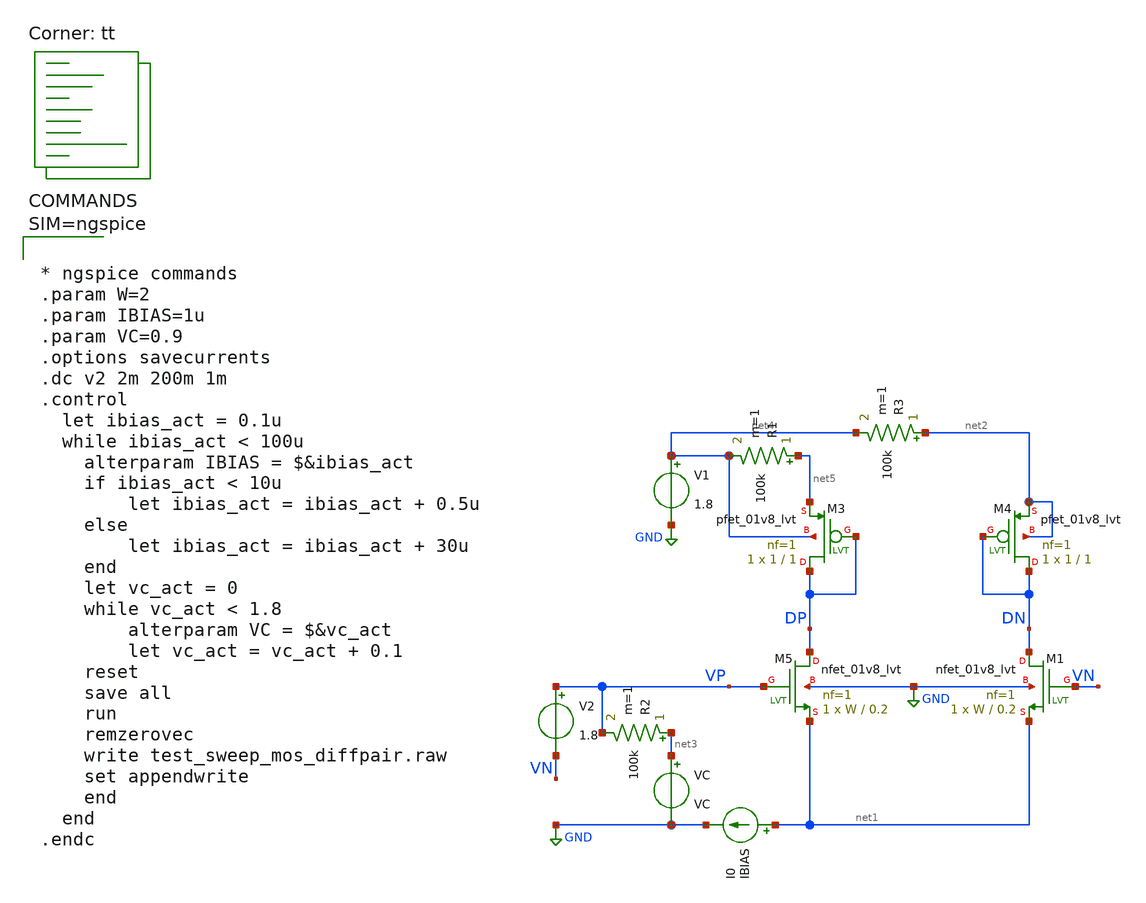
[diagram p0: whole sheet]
** sch_path: xschem/test_sweep_mos_diffpair.sch
* Copyright 2021 Stefan Frederik Schippers
* Licensed under the Apache License, Version 2.0 (the "License");
* you may not use this file except in compliance with the License.
* You may obtain a copy of the License at
* https://www.apache.org/licenses/LICENSE-2.0
* Unless required by applicable law or agreed to in writing, software
* distributed under the License is distributed on an "AS IS" BASIS,
* WITHOUT WARRANTIES OR CONDITIONS OF ANY KIND, either express or implied.
* See the License for the specific language governing permissions and
* limitations under the License.
**.subckt test_sweep_mos_diffpair
V1 net4 GND 1.8
V2 VP VN 1.8
I0 net1 GND IBIAS
XM3 DP DP net5 net4 sky130_fd_pr__pfet_01v8_lvt L=1 W=1 nf=1 ad='int((nf+1)/2) * W/nf * 0.29' as='int((nf+2)/2) * W/nf * 0.29'
+ pd='2*int((nf+1)/2) * (W/nf + 0.29)' ps='2*int((nf+2)/2) * (W/nf + 0.29)' nrd='0.29 / W' nrs='0.29 / W'
+ sa=0 sb=0 sd=0 mult=1 m=1
XM4 DN DN net2 net2 sky130_fd_pr__pfet_01v8_lvt L=1 W=1 nf=1 ad='int((nf+1)/2) * W/nf * 0.29' as='int((nf+2)/2) * W/nf * 0.29'
+ pd='2*int((nf+1)/2) * (W/nf + 0.29)' ps='2*int((nf+2)/2) * (W/nf + 0.29)' nrd='0.29 / W' nrs='0.29 / W'
+ sa=0 sb=0 sd=0 mult=1 m=1
R2 net3 VP 100k m=1
VC net3 GND VC
XM5 DP VP net1 GND sky130_fd_pr__nfet_01v8_lvt L=0.2 W=W nf=1 ad='int((nf+1)/2) * W/nf * 0.29' as='int((nf+2)/2) * W/nf * 0.29'
+ pd='2*int((nf+1)/2) * (W/nf + 0.29)' ps='2*int((nf+2)/2) * (W/nf + 0.29)' nrd='0.29 / W' nrs='0.29 / W'
+ sa=0 sb=0 sd=0 mult=1 m=1
XM1 DN VN net1 GND sky130_fd_pr__nfet_01v8_lvt L=0.2 W=W nf=1 ad='int((nf+1)/2) * W/nf * 0.29' as='int((nf+2)/2) * W/nf * 0.29'
+ pd='2*int((nf+1)/2) * (W/nf + 0.29)' ps='2*int((nf+2)/2) * (W/nf + 0.29)' nrd='0.29 / W' nrs='0.29 / W'
+ sa=0 sb=0 sd=0 mult=1 m=1
R1 net5 net4 100k m=1
R3 net2 net4 100k m=1
**** begin user architecture code
.lib $::SKYWATER_MODELS/sky130.lib.spice tt



* ngspice commands
.param W=2
.param IBIAS=1u
.param VC=0.9
.options savecurrents
.dc v2 2m 200m 1m
.control
  let ibias_act = 0.1u
  while ibias_act < 100u
    alterparam IBIAS = $&ibias_act
    if ibias_act < 10u
    	let ibias_act = ibias_act + 0.5u
    else
    	let ibias_act = ibias_act + 30u
    end
    let vc_act = 0
    while vc_act < 1.8
    	alterparam VC = $&vc_act
    	let vc_act = vc_act + 0.1
	reset
	save all
	run
	remzerovec
	write test_sweep_mos_diffpair.raw
	set appendwrite
    end
  end
.endc



**** end user architecture code
**.ends
.GLOBAL GND
.end
